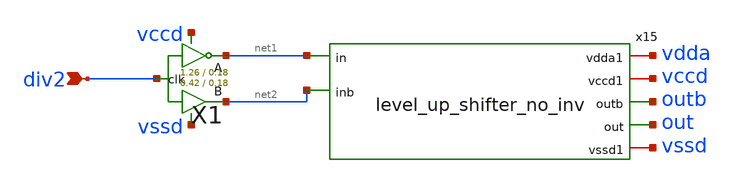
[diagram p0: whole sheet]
** sch_path: xschem/clkgen/level_up_shifter_d_a_x.sch
**.subckt level_up_shifter_d_a_x div2
*.ipin div2
X1 div2 net1 net2 vccd vssd comp_clks_1stage Wpmos=1.26 Lpmos=0.18 Wnmos=0.42 Lnmos=0.18
x15 vdda vccd net1 outb out vssd net2 level_up_shifter_no_inv
**.ends

* expanding   symbol:  clkgen/comp_clks_1stage.sym # of pins=5
** sym_path: xschem/clkgen/comp_clks_1stage.sym
** sch_path: xschem/clkgen/comp_clks_1stage.sch
.subckt comp_clks_1stage clk clka clkb vdd vss  Wpmos=1.26 Lpmos=0.18 Wnmos=0.42 Lnmos=0.18
*.ipin clk
*.opin clka
*.opin clkb
*.iopin vdd
*.iopin vss
X1 clk clka vdd vss inv Wpmos=Wpmos Lpmos=Lpmos Wnmos=Wnmos Lnmos=Lnmos
x2 clk clkb vss vdd vdd vss tg Wpmos=0.63 Lpmos=0.18 Wnmos=0.42 Lnmos=0.18
.ends


* expanding   symbol:  level_shifter/level_up_shifter_no_inv.sym # of pins=7
** sym_path: xschem/level_shifter/level_up_shifter_no_inv.sym
** sch_path: xschem/level_shifter/level_up_shifter_no_inv.sch
.subckt level_up_shifter_no_inv vdda1 vccd1 in outb out vssd1 inb
*.ipin in
*.iopin vdda1
*.opin out
*.opin outb
*.ipin inb
*.iopin vssd1
*.iopin vccd1
XM7 outb out vdda1 vdda1 sky130_fd_pr__pfet_01v8 L=0.15 W=0.42 nf=1 ad='int((nf+1)/2) * W/nf * 0.29'
+ as='int((nf+2)/2) * W/nf * 0.29' pd='2*int((nf+1)/2) * (W/nf + 0.29)' ps='2*int((nf+2)/2) * (W/nf + 0.29)'
+ nrd='0.29 / W' nrs='0.29 / W' sa=0 sb=0 sd=0 mult=1 m=1
XM8 out outb vdda1 vdda1 sky130_fd_pr__pfet_01v8 L=0.15 W=0.42 nf=1 ad='int((nf+1)/2) * W/nf * 0.29'
+ as='int((nf+2)/2) * W/nf * 0.29' pd='2*int((nf+1)/2) * (W/nf + 0.29)' ps='2*int((nf+2)/2) * (W/nf + 0.29)'
+ nrd='0.29 / W' nrs='0.29 / W' sa=0 sb=0 sd=0 mult=1 m=1
XM2 outb inb vdda1 vssd1 sky130_fd_pr__nfet_01v8 L=0.15 W=0.6 nf=1 ad='int((nf+1)/2) * W/nf * 0.29' as='int((nf+2)/2) * W/nf * 0.29'
+ pd='2*int((nf+1)/2) * (W/nf + 0.29)' ps='2*int((nf+2)/2) * (W/nf + 0.29)' nrd='0.29 / W' nrs='0.29 / W'
+ sa=0 sb=0 sd=0 mult=4 m=4
XM3 outb in vssd1 vssd1 sky130_fd_pr__nfet_01v8 L=0.15 W=0.6 nf=1 ad='int((nf+1)/2) * W/nf * 0.29' as='int((nf+2)/2) * W/nf * 0.29'
+ pd='2*int((nf+1)/2) * (W/nf + 0.29)' ps='2*int((nf+2)/2) * (W/nf + 0.29)' nrd='0.29 / W' nrs='0.29 / W'
+ sa=0 sb=0 sd=0 mult=4 m=4
XM4 vssd1 in outb vssd1 sky130_fd_pr__nfet_01v8 L=0.15 W=0.6 nf=1 ad='int((nf+1)/2) * W/nf * 0.29' as='int((nf+2)/2) * W/nf * 0.29'
+ pd='2*int((nf+1)/2) * (W/nf + 0.29)' ps='2*int((nf+2)/2) * (W/nf + 0.29)' nrd='0.29 / W' nrs='0.29 / W'
+ sa=0 sb=0 sd=0 mult=4 m=4
XM5 out inb vssd1 vssd1 sky130_fd_pr__nfet_01v8 L=0.15 W=0.6 nf=1 ad='int((nf+1)/2) * W/nf * 0.29' as='int((nf+2)/2) * W/nf * 0.29'
+ pd='2*int((nf+1)/2) * (W/nf + 0.29)' ps='2*int((nf+2)/2) * (W/nf + 0.29)' nrd='0.29 / W' nrs='0.29 / W'
+ sa=0 sb=0 sd=0 mult=4 m=4
XM6 vssd1 inb out vssd1 sky130_fd_pr__nfet_01v8 L=0.15 W=0.6 nf=1 ad='int((nf+1)/2) * W/nf * 0.29' as='int((nf+2)/2) * W/nf * 0.29'
+ pd='2*int((nf+1)/2) * (W/nf + 0.29)' ps='2*int((nf+2)/2) * (W/nf + 0.29)' nrd='0.29 / W' nrs='0.29 / W'
+ sa=0 sb=0 sd=0 mult=4 m=4
XM9 vdda1 in out vssd1 sky130_fd_pr__nfet_01v8 L=0.15 W=0.6 nf=1 ad='int((nf+1)/2) * W/nf * 0.29' as='int((nf+2)/2) * W/nf * 0.29'
+ pd='2*int((nf+1)/2) * (W/nf + 0.29)' ps='2*int((nf+2)/2) * (W/nf + 0.29)' nrd='0.29 / W' nrs='0.29 / W'
+ sa=0 sb=0 sd=0 mult=4 m=4
XM10 out in vdda1 vssd1 sky130_fd_pr__nfet_01v8 L=0.15 W=0.6 nf=1 ad='int((nf+1)/2) * W/nf * 0.29' as='int((nf+2)/2) * W/nf * 0.29'
+ pd='2*int((nf+1)/2) * (W/nf + 0.29)' ps='2*int((nf+2)/2) * (W/nf + 0.29)' nrd='0.29 / W' nrs='0.29 / W'
+ sa=0 sb=0 sd=0 mult=4 m=4
XM11 vdda1 inb outb vssd1 sky130_fd_pr__nfet_01v8 L=0.15 W=0.6 nf=1 ad='int((nf+1)/2) * W/nf * 0.29'
+ as='int((nf+2)/2) * W/nf * 0.29' pd='2*int((nf+1)/2) * (W/nf + 0.29)' ps='2*int((nf+2)/2) * (W/nf + 0.29)'
+ nrd='0.29 / W' nrs='0.29 / W' sa=0 sb=0 sd=0 mult=4 m=4
.ends


* expanding   symbol:  inv/inv.sym # of pins=4
** sym_path: xschem/inv/inv.sym
** sch_path: xschem/inv/inv.sch
.subckt inv in out vdd vss  Wpmos=Wpmos Lpmos=Lpmos Wnmos=Wnmos Lnmos=Lnmos
*.ipin in
*.iopin out
*.iopin vdd
*.iopin vss
XM1 vss in out vss sky130_fd_pr__nfet_01v8 L=Lnmos W=Wnmos nf=1 ad='int((nf+1)/2) * W/nf * 0.29' as='int((nf+2)/2) * W/nf * 0.29'
+ pd='2*int((nf+1)/2) * (W/nf + 0.29)' ps='2*int((nf+2)/2) * (W/nf + 0.29)' nrd='0.29 / W' nrs='0.29 / W'
+ sa=0 sb=0 sd=0 mult=1 m=1
XM2 vdd in out vdd sky130_fd_pr__pfet_01v8 L=Lpmos W=Wpmos nf=1 ad='int((nf+1)/2) * W/nf * 0.29' as='int((nf+2)/2) * W/nf * 0.29'
+ pd='2*int((nf+1)/2) * (W/nf + 0.29)' ps='2*int((nf+2)/2) * (W/nf + 0.29)' nrd='0.29 / W' nrs='0.29 / W'
+ sa=0 sb=0 sd=0 mult=1 m=1
.ends


* expanding   symbol:  xschem/transmission_gate/tg.sym # of pins=6
** sym_path: xschem/transmission_gate/tg.sym
** sch_path: xschem/transmission_gate/tg.sch
.subckt tg in out ctrl_ ctrl vdda vssa  Wpmos=0.42 Lpmos=0.18 Wnmos=0.42 Lnmos=0.18
*.iopin in
*.iopin out
*.ipin ctrl_
*.ipin ctrl
*.ipin vdda
*.ipin vssa
XM1 out ctrl in vssa sky130_fd_pr__nfet_01v8 L=Lnmos W=Wnmos nf=1 ad='int((nf+1)/2) * W/nf * 0.29' as='int((nf+2)/2) * W/nf * 0.29'
+ pd='2*int((nf+1)/2) * (W/nf + 0.29)' ps='2*int((nf+2)/2) * (W/nf + 0.29)' nrd='0.29 / W' nrs='0.29 / W'
+ sa=0 sb=0 sd=0 mult=1 m=1
XM2 out ctrl_ in vdda sky130_fd_pr__pfet_01v8 L=Lpmos W=Wpmos nf=1 ad='int((nf+1)/2) * W/nf * 0.29' as='int((nf+2)/2) * W/nf * 0.29'
+ pd='2*int((nf+1)/2) * (W/nf + 0.29)' ps='2*int((nf+2)/2) * (W/nf + 0.29)' nrd='0.29 / W' nrs='0.29 / W'
+ sa=0 sb=0 sd=0 mult=2 m=2
.ends

.end
